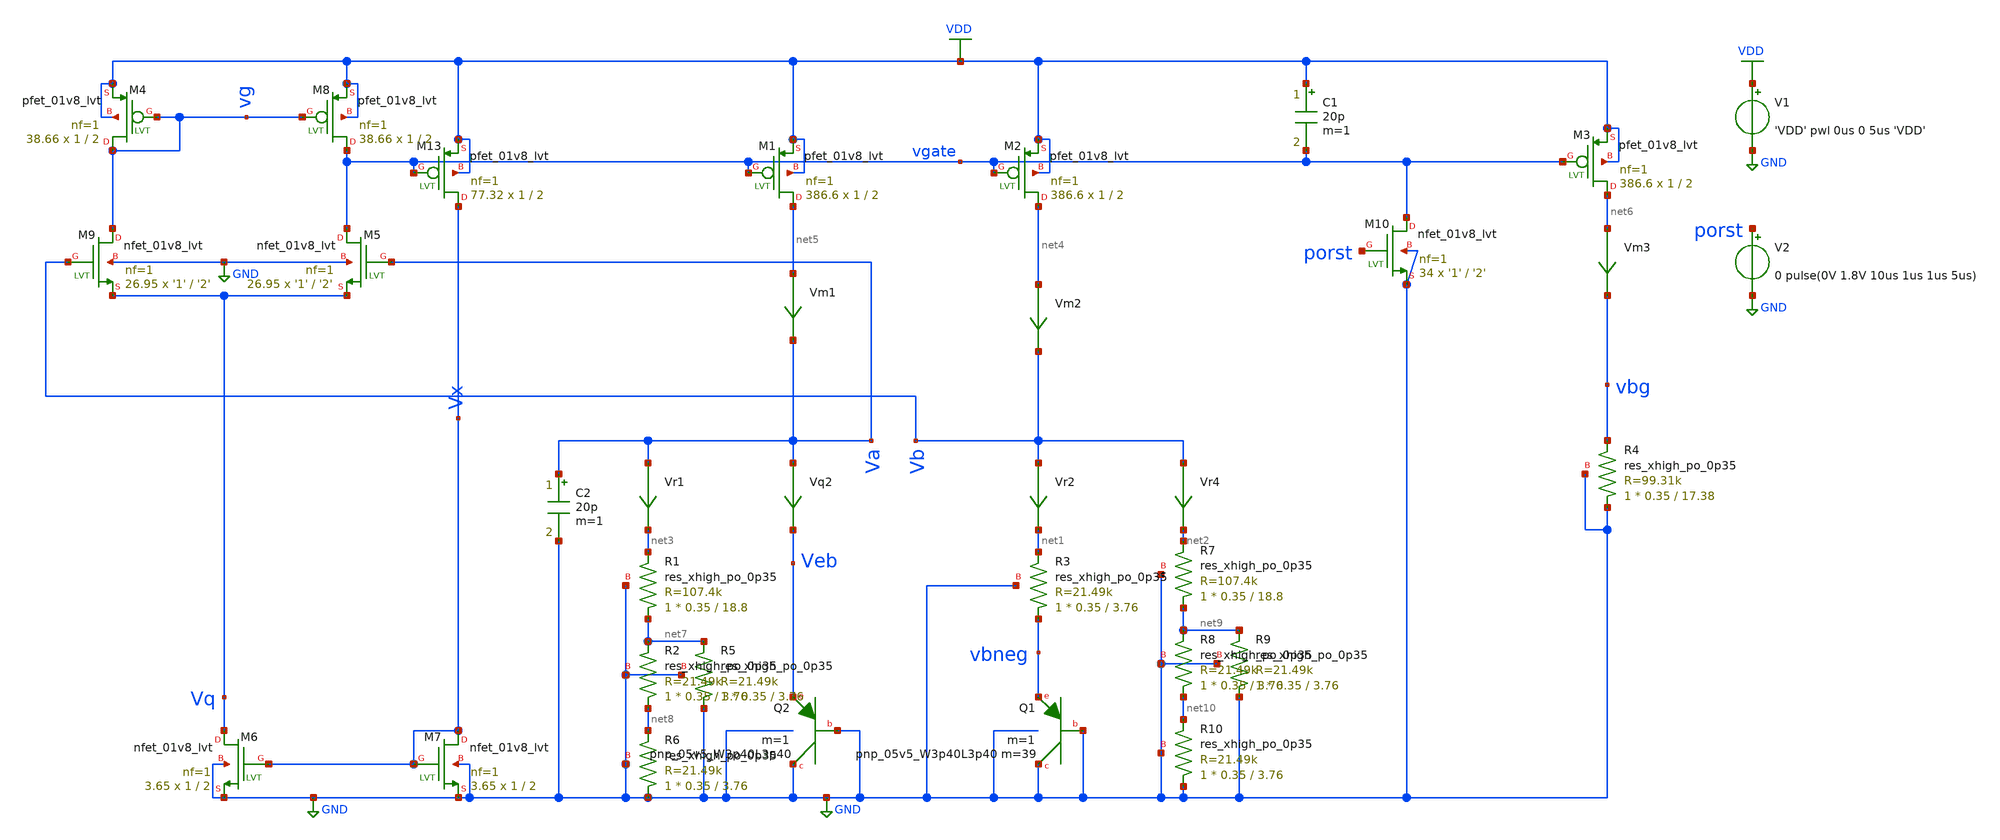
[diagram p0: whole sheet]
** sch_path: schematics/tsmc_bandgap_real_tran_adjusted_res.sch
**.subckt tsmc_bandgap_real_tran_adjusted_res
V1 VDD GND 'VDD' pwl 0us 0 5us 'VDD'
XQ2 GND GND Veb sky130_fd_pr__pnp_05v5_W3p40L3p40 m=1
Vr4 Vb net2 0
.save i(vr4)
Vr2 Vb net1 0
.save i(vr2)
Vm1 net5 Va 0
.save i(vm1)
Vm2 net4 Vb 0
.save i(vm2)
Vm3 net6 vbg 0
.save i(vm3)
Vr1 Va net3 0
.save i(vr1)
Vq2 Va Veb 0
.save i(vq2)
XQ1 GND GND vbneg sky130_fd_pr__pnp_05v5_W3p40L3p40 m=39 m=1
XM5 vgate Va Vq GND sky130_fd_pr__nfet_01v8_lvt L='2' W='1' nf=1 ad='int((nf+1)/2) * W/nf * 0.29' as='int((nf+2)/2) * W/nf * 0.29'
+ pd='2*int((nf+1)/2) * (W/nf + 0.29)' ps='2*int((nf+2)/2) * (W/nf + 0.29)' nrd='0.29 / W' nrs='0.29 / W'
+ sa=0 sb=0 sd=0 mult=26.95 m=26.95
XM6 Vq Vx GND GND sky130_fd_pr__nfet_01v8_lvt L=2 W=1 nf=1 ad='int((nf+1)/2) * W/nf * 0.29' as='int((nf+2)/2) * W/nf * 0.29'
+ pd='2*int((nf+1)/2) * (W/nf + 0.29)' ps='2*int((nf+2)/2) * (W/nf + 0.29)' nrd='0.29 / W' nrs='0.29 / W'
+ sa=0 sb=0 sd=0 mult=3.65 m=3.65
XM9 vg Vb Vq GND sky130_fd_pr__nfet_01v8_lvt L='2' W='1' nf=1 ad='int((nf+1)/2) * W/nf * 0.29' as='int((nf+2)/2) * W/nf * 0.29'
+ pd='2*int((nf+1)/2) * (W/nf + 0.29)' ps='2*int((nf+2)/2) * (W/nf + 0.29)' nrd='0.29 / W' nrs='0.29 / W'
+ sa=0 sb=0 sd=0 mult=26.95 m=26.95
XM7 Vx Vx GND GND sky130_fd_pr__nfet_01v8_lvt L=2 W=1 nf=1 ad='int((nf+1)/2) * W/nf * 0.29' as='int((nf+2)/2) * W/nf * 0.29'
+ pd='2*int((nf+1)/2) * (W/nf + 0.29)' ps='2*int((nf+2)/2) * (W/nf + 0.29)' nrd='0.29 / W' nrs='0.29 / W'
+ sa=0 sb=0 sd=0 mult=3.65 m=3.65
XM13 Vx vgate VDD VDD sky130_fd_pr__pfet_01v8_lvt L=2 W=1 nf=1 ad='int((nf+1)/2) * W/nf * 0.29' as='int((nf+2)/2) * W/nf * 0.29'
+ pd='2*int((nf+1)/2) * (W/nf + 0.29)' ps='2*int((nf+2)/2) * (W/nf + 0.29)' nrd='0.29 / W' nrs='0.29 / W'
+ sa=0 sb=0 sd=0 mult=77.32 m=77.32
XM1 net5 vgate VDD VDD sky130_fd_pr__pfet_01v8_lvt L=2 W=1 nf=1 ad='int((nf+1)/2) * W/nf * 0.29' as='int((nf+2)/2) * W/nf * 0.29'
+ pd='2*int((nf+1)/2) * (W/nf + 0.29)' ps='2*int((nf+2)/2) * (W/nf + 0.29)' nrd='0.29 / W' nrs='0.29 / W'
+ sa=0 sb=0 sd=0 mult=386.6 m=386.6
XM2 net4 vgate VDD VDD sky130_fd_pr__pfet_01v8_lvt L=2 W=1 nf=1 ad='int((nf+1)/2) * W/nf * 0.29' as='int((nf+2)/2) * W/nf * 0.29'
+ pd='2*int((nf+1)/2) * (W/nf + 0.29)' ps='2*int((nf+2)/2) * (W/nf + 0.29)' nrd='0.29 / W' nrs='0.29 / W'
+ sa=0 sb=0 sd=0 mult=386.6 m=386.6
XM3 net6 vgate VDD VDD sky130_fd_pr__pfet_01v8_lvt L=2 W=1 nf=1 ad='int((nf+1)/2) * W/nf * 0.29' as='int((nf+2)/2) * W/nf * 0.29'
+ pd='2*int((nf+1)/2) * (W/nf + 0.29)' ps='2*int((nf+2)/2) * (W/nf + 0.29)' nrd='0.29 / W' nrs='0.29 / W'
+ sa=0 sb=0 sd=0 mult=386.6 m=386.6
XR3 vbneg net1 GND sky130_fd_pr__res_xhigh_po_0p35 L=3.76 mult=1 m=1
XR4 GND vbg GND sky130_fd_pr__res_xhigh_po_0p35 L=17.38 mult=1 m=1
XM4 vg vg VDD VDD sky130_fd_pr__pfet_01v8_lvt L=2 W=1 nf=1 ad='int((nf+1)/2) * W/nf * 0.29' as='int((nf+2)/2) * W/nf * 0.29'
+ pd='2*int((nf+1)/2) * (W/nf + 0.29)' ps='2*int((nf+2)/2) * (W/nf + 0.29)' nrd='0.29 / W' nrs='0.29 / W'
+ sa=0 sb=0 sd=0 mult=38.66 m=38.66
XM8 vgate vg VDD VDD sky130_fd_pr__pfet_01v8_lvt L=2 W=1 nf=1 ad='int((nf+1)/2) * W/nf * 0.29' as='int((nf+2)/2) * W/nf * 0.29'
+ pd='2*int((nf+1)/2) * (W/nf + 0.29)' ps='2*int((nf+2)/2) * (W/nf + 0.29)' nrd='0.29 / W' nrs='0.29 / W'
+ sa=0 sb=0 sd=0 mult=38.66 m=38.66
XM10 vgate porst GND GND sky130_fd_pr__nfet_01v8_lvt L='2' W='1' nf=1 ad='int((nf+1)/2) * W/nf * 0.29'
+ as='int((nf+2)/2) * W/nf * 0.29' pd='2*int((nf+1)/2) * (W/nf + 0.29)' ps='2*int((nf+2)/2) * (W/nf + 0.29)'
+ nrd='0.29 / W' nrs='0.29 / W' sa=0 sb=0 sd=0 mult=34 m=34
V2 porst GND 0 pulse(0V 1.8V 10us 1us 1us 5us)
C1 VDD vgate 20p m=1
C2 Va GND 20p m=1
XR1 net7 net3 GND sky130_fd_pr__res_xhigh_po_0p35 L=18.8 mult=1 m=1
XR2 net8 net7 GND sky130_fd_pr__res_xhigh_po_0p35 L=3.76 mult=1 m=1
XR5 GND net7 GND sky130_fd_pr__res_xhigh_po_0p35 L=3.76 mult=1 m=1
XR6 GND net8 GND sky130_fd_pr__res_xhigh_po_0p35 L=3.76 mult=1 m=1
XR7 net9 net2 GND sky130_fd_pr__res_xhigh_po_0p35 L=18.8 mult=1 m=1
XR8 net10 net9 GND sky130_fd_pr__res_xhigh_po_0p35 L=3.76 mult=1 m=1
XR9 GND net9 GND sky130_fd_pr__res_xhigh_po_0p35 L=3.76 mult=1 m=1
XR10 GND net10 GND sky130_fd_pr__res_xhigh_po_0p35 L=3.76 mult=1 m=1
**** begin user architecture code

.include $::SKYWATER_MODELS/cells/nfet_01v8/sky130_fd_pr__nfet_01v8__tt.corner.spice
.include $::SKYWATER_MODELS/cells/nfet_01v8_lvt/sky130_fd_pr__nfet_01v8_lvt__tt.corner.spice
.include $::SKYWATER_MODELS/cells/pfet_01v8/sky130_fd_pr__pfet_01v8__tt.corner.spice
.include $::SKYWATER_MODELS/cells/nfet_03v3_nvt/sky130_fd_pr__nfet_03v3_nvt__tt.corner.spice
.include $::SKYWATER_MODELS/cells/nfet_05v0_nvt/sky130_fd_pr__nfet_05v0_nvt__tt.corner.spice
.include $::SKYWATER_MODELS/cells/esd_nfet_01v8/sky130_fd_pr__esd_nfet_01v8__tt.corner.spice
.include $::SKYWATER_MODELS/cells/pfet_01v8_lvt/sky130_fd_pr__pfet_01v8_lvt__tt.corner.spice
.include $::SKYWATER_MODELS/cells/pfet_01v8_hvt/sky130_fd_pr__pfet_01v8_hvt__tt.corner.spice
.include $::SKYWATER_MODELS/cells/esd_pfet_g5v0d10v5/sky130_fd_pr__esd_pfet_g5v0d10v5__tt.corner.spice
.include $::SKYWATER_MODELS/cells/pfet_g5v0d10v5/sky130_fd_pr__pfet_g5v0d10v5__tt.corner.spice
.include $::SKYWATER_MODELS/cells/pfet_g5v0d16v0/sky130_fd_pr__pfet_g5v0d16v0__tt.corner.spice
.include $::SKYWATER_MODELS/cells/nfet_g5v0d10v5/sky130_fd_pr__nfet_g5v0d10v5__tt.corner.spice
.include $::SKYWATER_MODELS/cells/nfet_g5v0d16v0/sky130_fd_pr__nfet_g5v0d16v0__tt_discrete.corner.spice
.include $::SKYWATER_MODELS/cells/esd_nfet_g5v0d10v5/sky130_fd_pr__esd_nfet_g5v0d10v5__tt.corner.spice
.include $::SKYWATER_MODELS/models/corners/tt/nonfet.spice
* Mismatch parameters
.include $::SKYWATER_MODELS/cells/nfet_01v8/sky130_fd_pr__nfet_01v8__mismatch.corner.spice
.include $::SKYWATER_MODELS/cells/pfet_01v8/sky130_fd_pr__pfet_01v8__mismatch.corner.spice
.include $::SKYWATER_MODELS/cells/nfet_01v8_lvt/sky130_fd_pr__nfet_01v8_lvt__mismatch.corner.spice
.include $::SKYWATER_MODELS/cells/pfet_01v8_lvt/sky130_fd_pr__pfet_01v8_lvt__mismatch.corner.spice
.include $::SKYWATER_MODELS/cells/pfet_01v8_hvt/sky130_fd_pr__pfet_01v8_hvt__mismatch.corner.spice
.include $::SKYWATER_MODELS/cells/nfet_g5v0d10v5/sky130_fd_pr__nfet_g5v0d10v5__mismatch.corner.spice
.include $::SKYWATER_MODELS/cells/pfet_g5v0d10v5/sky130_fd_pr__pfet_g5v0d10v5__mismatch.corner.spice
.include $::SKYWATER_MODELS/cells/nfet_05v0_nvt/sky130_fd_pr__nfet_05v0_nvt__mismatch.corner.spice
.include $::SKYWATER_MODELS/cells/nfet_03v3_nvt/sky130_fd_pr__nfet_03v3_nvt__mismatch.corner.spice
* Resistor$::SKYWATER_MODELS/Capacitor
.include $::SKYWATER_MODELS/models/r+c/res_typical__cap_typical.spice
.include $::SKYWATER_MODELS/models/r+c/res_typical__cap_typical__lin.spice
* Special cells
.include $::SKYWATER_MODELS/models/corners/tt/specialized_cells.spice
* All models
.include $::SKYWATER_MODELS/models/all.spice
.include $::SKYWATER_MODELS/cells/pnp_05v5/sky130_fd_pr__pnp_05v5_W3p40L3p40.model.spice
* Corner
.include $::SKYWATER_MODELS/models/corners/tt/rf.spice



.option savecurrents
.param R3val='22.187k'
.param alpha='1'
.param R2R3ratio='5.6555038*alpha'
.param R2val='R3val*R2R3ratio'
.param R4R2ratio='0.79694273'
.param R4val='R2val*R4R2ratio
.param VDD=1.8
.control
save all  @m.xm1.msky130_fd_pr__pfet_01v8_lvt[gm]  @m.xm2.msky130_fd_pr__pfet_01v8_lvt[gm]  @m.xm3.msky130_fd_pr__pfet_01v8_lvt[gm]  @m.xm4.msky130_fd_pr__pfet_01v8_lvt[gm]  @m.xm5.msky130_fd_pr__nfet_01v8_lvt[gm]  @m.xm6.msky130_fd_pr__nfet_01v8_lvt[gm]  @m.xm7.msky130_fd_pr__nfet_01v8_lvt[gm]  @m.xm8.msky130_fd_pr__pfet_01v8_lvt[gm]  @m.xm9.msky130_fd_pr__nfet_01v8_lvt[gm]  @m.xm13.msky130_fd_pr__pfet_01v8_lvt[gm]

option temp=27
tran 0.1n 20u
option temp=0
tran 0.1n 20u
option temp=70
tran 0.1n 20u
write ./sims/tsmc_bandgap_real_adj_res_70degc_vbg.raw vbg
setplot tran2
write ./sims/tsmc_bandgap_real_adj_res_0degc_vbg.raw vbg
setplot tran1
write ./sims/tsmc_bandgap_real_adj_res_27degc_vbg.raw vbg
unset askquit
quit
.endc


**** end user architecture code
**.ends
.GLOBAL VDD
.GLOBAL GND
.end
